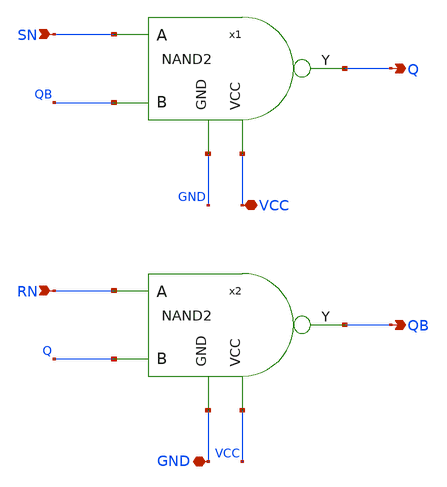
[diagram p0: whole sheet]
** sch_path: blocks/03_StrongARM/xschem/SR_Latch.sch
**.subckt SR_Latch SN RN Q QB VCC GND
*.ipin SN
*.ipin RN
*.opin Q
*.opin QB
*.iopin VCC
*.iopin GND
x1 SN QB Q GND VCC NAND2
x2 RN Q QB GND VCC NAND2
**.ends

* expanding   symbol:  blocks/03_StrongARM/xschem/NAND2.sym # of pins=5
** sym_path: blocks/03_StrongARM/xschem/NAND2.sym
** sch_path: blocks/03_StrongARM/xschem/NAND2.sch
.subckt NAND2 A B Y GND VCC
*.ipin A
*.ipin B
*.opin Y
*.iopin GND
*.iopin VCC
XMP1 Y A VCC VCC sky130_fd_pr__pfet_01v8 L=0.15 W=2 nf=1 ad='int((1 + 1)/2) * 2 / 1 * 0.29' as='int((1 + 2)/2) * 2 / 1 * 0.29'
+ pd='2*int((1 + 1)/2) * (2 / 1 + 0.29)' ps='2*int((1 + 2)/2) * (2 / 1 + 0.29)' nrd='0.29 / 2 ' nrs='0.29 / 2 '
+ sa=0 sb=0 sd=0 mult=1 m=1
XMP2 Y B VCC VCC sky130_fd_pr__pfet_01v8 L=0.15 W=2 nf=1 ad='int((1 + 1)/2) * 2 / 1 * 0.29' as='int((1 + 2)/2) * 2 / 1 * 0.29'
+ pd='2*int((1 + 1)/2) * (2 / 1 + 0.29)' ps='2*int((1 + 2)/2) * (2 / 1 + 0.29)' nrd='0.29 / 2 ' nrs='0.29 / 2 '
+ sa=0 sb=0 sd=0 mult=1 m=1
XMN1 Y A net1 GND sky130_fd_pr__nfet_01v8 L=0.15 W=2 nf=1 ad='int((1 + 1)/2) * 2 / 1 * 0.29' as='int((1 + 2)/2) * 2 / 1 * 0.29'
+ pd='2*int((1 + 1)/2) * (2 / 1 + 0.29)' ps='2*int((1 + 2)/2) * (2 / 1 + 0.29)' nrd='0.29 / 2 ' nrs='0.29 / 2 '
+ sa=0 sb=0 sd=0 mult=1 m=1
XMN2 net1 B GND GND sky130_fd_pr__nfet_01v8 L=0.15 W=2 nf=1 ad='int((1 + 1)/2) * 2 / 1 * 0.29' as='int((1 + 2)/2) * 2 / 1 * 0.29'
+ pd='2*int((1 + 1)/2) * (2 / 1 + 0.29)' ps='2*int((1 + 2)/2) * (2 / 1 + 0.29)' nrd='0.29 / 2 ' nrs='0.29 / 2 '
+ sa=0 sb=0 sd=0 mult=1 m=1
.ends

.end
